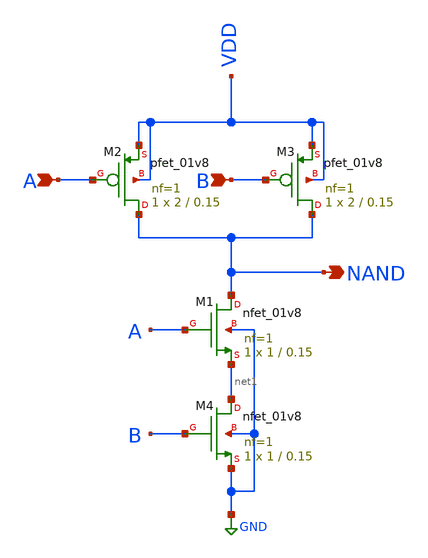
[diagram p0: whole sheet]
** sch_path: skywater_stuff/NAND.sch
**.subckt NAND A B NAND
*.ipin A
*.ipin B
*.opin NAND
XM1 NAND A net1 GND sky130_fd_pr__nfet_01v8 L=0.15 W=1 nf=1 ad='int((nf+1)/2) * W/nf * 0.29' as='int((nf+2)/2) * W/nf * 0.29'
+ pd='2*int((nf+1)/2) * (W/nf + 0.29)' ps='2*int((nf+2)/2) * (W/nf + 0.29)' nrd='0.29 / W' nrs='0.29 / W'
+ sa=0 sb=0 sd=0 mult=1 m=1
XM2 NAND A VDD VDD sky130_fd_pr__pfet_01v8 L=0.15 W=2 nf=1 ad='int((nf+1)/2) * W/nf * 0.29' as='int((nf+2)/2) * W/nf * 0.29'
+ pd='2*int((nf+1)/2) * (W/nf + 0.29)' ps='2*int((nf+2)/2) * (W/nf + 0.29)' nrd='0.29 / W' nrs='0.29 / W'
+ sa=0 sb=0 sd=0 mult=1 m=1
XM3 NAND B VDD VDD sky130_fd_pr__pfet_01v8 L=0.15 W=2 nf=1 ad='int((nf+1)/2) * W/nf * 0.29' as='int((nf+2)/2) * W/nf * 0.29'
+ pd='2*int((nf+1)/2) * (W/nf + 0.29)' ps='2*int((nf+2)/2) * (W/nf + 0.29)' nrd='0.29 / W' nrs='0.29 / W'
+ sa=0 sb=0 sd=0 mult=1 m=1
XM4 net1 B GND GND sky130_fd_pr__nfet_01v8 L=0.15 W=1 nf=1 ad='int((nf+1)/2) * W/nf * 0.29' as='int((nf+2)/2) * W/nf * 0.29'
+ pd='2*int((nf+1)/2) * (W/nf + 0.29)' ps='2*int((nf+2)/2) * (W/nf + 0.29)' nrd='0.29 / W' nrs='0.29 / W'
+ sa=0 sb=0 sd=0 mult=1 m=1
**.ends
.GLOBAL GND
.end
